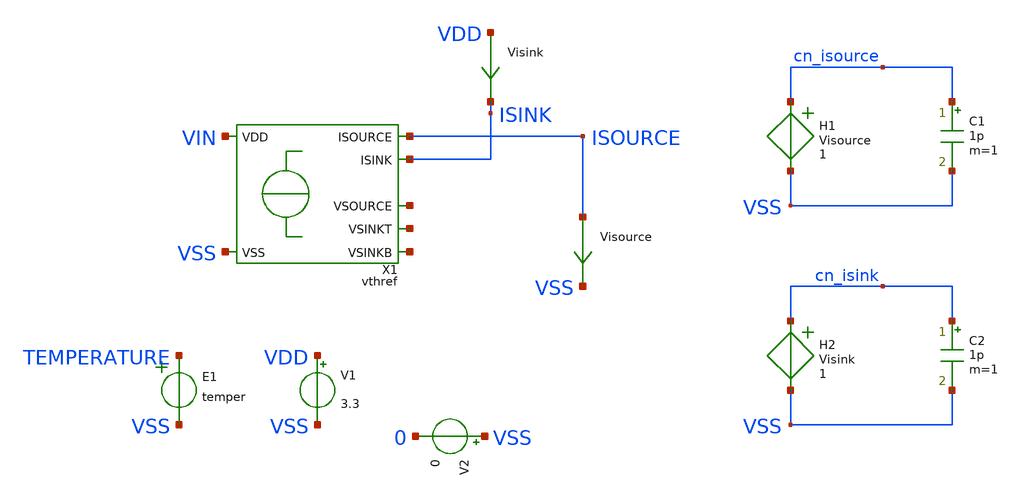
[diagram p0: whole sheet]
** sch_path: ip/vthref/xschem/vthref_tb.sch
**.subckt vthref_tb
X1 VIN VSS ISOURCE ISINK net1 net3 net2 vthref
V1 VDD VSS 3.3
Visink VDD ISINK 0
.save i(visink)
Visource ISOURCE VSS 0
.save i(visource)
V2 VSS 0 0
C1 cn_isource VSS 1p m=1
C2 cn_isink VSS 1p m=1
H1 cn_isource VSS Visource 1
H2 cn_isink VSS Visink 1
E1 TEMPERATURE VSS VOL=' temper '
**** begin user architecture code


.csparam TB_ID=${::TB_ID}
.csparam MC_RUNS=${::MC_RUNS}
.csparam EXIT_NGSPICE=${::EXIT_NGSPICE}
.lib ${::IHP_MODELS}/sg13g2.lib ${::CORNER}



* this experimental option enables mos model bin
* selection based on W/NF instead of W
.option wnflag=0

Vac1 VIN VDD 0.0 AC 1

Vdummy Vsweep VSS 0.0

.nodeset v(x1.vp)=1.0
.nodeset v(x1.vth)=0.22
.nodeset v(x1.vm)=0.840
.nodeset v(x1.vs)=0.006

.control
* option savecurrents
save all


* dummy block for goto
if (1)
if TB_ID = 0
	goto DC
end
if TB_ID = 1
	goto DC
end
if TB_ID = 2
	goto SINK_NOISE
end
if TB_ID = 3
	goto SOURCE_NOISE
end
if TB_ID = 4
	goto TRAN_STARTUP
end
if TB_ID = 5
	goto DC_PEX
end

****************************************
label DC
save all @n.x1.xmvth.nsg13_lv_nmos[ise] @n.x1.xmsul.nsg13_hv_nmos[ide] @n.x1.xmfb.nsg13_hv_nmos[ise]
.include vthref.inc
label DC_PEX
*save all
****************************************
if MC_RUNS = 0
	let veclen=3
	let source_pp = vector(veclen)
	let sink_pp = vector(veclen)
	let source_min = vector(veclen)
	let source_max = vector(veclen)
	let sink_min = vector(veclen)
	let sink_max = vector(veclen)
	let myvdd = vector(veclen)
	let idx = 0
	foreach v_sweep 1.8 2.5 3.3
	*foreach v_sweep 2.5
  		alter v1=$v_sweep
		option reltol=0.0001
  		dc temp -40 125 1
  		plot visource#branch
  		plot visink#branch
  		*plot x1.vth
  		*plot x1.vp
  		*plot x1.vm
		*plot x1.vs
		plot v.x1.vmeas#branch v.x1.vmeas1#branch
		*plot v.x1.vmeas2#branch
		*plot -1*@n.x1.xmvth.nsg13_lv_nmos[ise] @n.x1.xmsul.nsg13_hv_nmos[ide]
+ -1*@n.x1.xmfb.nsg13_hv_nmos[ise]
		*plot @n.x1.xmvth.nsg13_lv_nmos[vds] @n.x1.xmfb.nsg13_hv_nmos[vds]
+ @n.x1.xmmir1l.nsg13_hv_pmos[vds] @n.x1.xmmir1r.nsg13_hv_pmos[vds]
		let source_min[idx] = minimum(visource#branch)
		let source_max[idx] = maximum(visource#branch)
		let source_pp[idx] = maximum(visource#branch)-minimum(visource#branch)
		let sink_min[idx] = minimum(visink#branch)
		let sink_max[idx] = maximum(visink#branch)
		let sink_pp[idx] = maximum(visink#branch)-minimum(visink#branch)
		let myvdd[idx] = $v_sweep
		let idx = idx + 1
		*echo ISOURCE span: $&source_pp[idx]
		*echo ISINK span: $&sink_pp[idx]
		write dc.raw all
		set appendwrite
	end
	set nobreak
	set width=300
	print myvdd, source_pp, sink_pp, source_min, source_max, sink_min, sink_max > dc.csv
else
	let source_pp = vector(MC_RUNS)
	let sink_pp = vector(MC_RUNS)
	let source_min = vector(MC_RUNS)
	let source_max = vector(MC_RUNS)
	let sink_min = vector(MC_RUNS)
	let sink_max = vector(MC_RUNS)
	let run=0
	dowhile run < MC_RUNS
		echo MC-RUN: $&run
		alter v1=aunif(2.55,0.75)
		option reltol=0.0001
		dc temp -40 140 1
		let source_min[run] = minimum(visource#branch)
		let source_max[run] = maximum(visource#branch)
		let source_pp[run] = maximum(visource#branch)-minimum(visource#branch)
		let sink_min[run] = minimum(visink#branch)
		let sink_max[run] = maximum(visink#branch)
		let sink_pp[run] = maximum(visink#branch)-minimum(visink#branch)
  		*plot visource#branch
		*plot visink#branch
		*write dc_CID_{$&CORNER_ID}_MC_{$&run}.raw all
 		reset
		let run = run + 1
	end
	set nobreak
	set width=300
	print source_pp, sink_pp, source_min, source_max, sink_min, sink_max > dc.csv
end
goto done

****************************************
label SOURCE_NOISE
****************************************
noise v(cn_isource) Vac1 dec 10 1 100e3 1
setplot noise2
print onoise_total
setplot noise1
plot onoise_spectrum
write noise1_isource.raw all
goto done

****************************************
label SINK_NOISE
****************************************
noise v(cn_isink) Vac1 dec 10 1 100e3 1
setplot noise2
print onoise_total
setplot noise1
plot onoise_spectrum loglog
write noise1_isink.raw all
goto done

****************************************
label TRAN_STARTUP
****************************************
if MC_RUNS = 0
	let veclen=3
	let startup_t = vector(veclen)
	let run=0
	foreach v_sweep 1.8 2.5 3.3
	*foreach v_sweep 3.3
		save all
		alter vdummy=$v_sweep
		alter @v1[pwl] = [ 0 0 1u 0 10u $v_sweep]
  		tran 10n 100u
  		plot visource#branch
  		plot visink#branch
		plot VDD
		meas tran m_cur_up when i(visource)=1e-6 rise=1
		let startup_t[run] = m_cur_up
		write tran.raw all
		let run = run + 1
		set appendwrite
		reset
	end
	print startup_t > tran.csv
else
	let startup_t = vector(MC_RUNS)
	let run=0
	dowhile run < MC_RUNS
		echo MC-RUN: $&run
		alter @v1[pwl] = [ 0 0 1u 0 10u 3.3]
		tran 10n 100u
		meas tran m_cur_up when i(visource)=1e-6 rise=1
		let startup_t[run] = m_cur_up
 		reset
		let run = run + 1
	end
	print startup_t > tran.csv
end
goto done

****************************************
label done
****************************************
if EXIT_NGSPICE > 0.0
	exit
end
end
.endc


**** end user architecture code
**.ends

* expanding   symbol:  vthref.sym # of pins=7
** sym_path: ip/vthref/xschem/vthref.sym
** sch_path: ip/vthref/xschem/vthref.sch
.subckt vthref VDD VSS ISOURCE ISINK VSOURCE VSINKT VSINKB
*.iopin VSS
*.iopin VDD
*.ipin ISINK
*.opin ISOURCE
*.iopin VSOURCE
*.iopin VSINKT
*.iopin VSINKB
XMMIR1L vp vm VDD VDD sg13_hv_pmos w=10u l=15u ng=1 m=6 mm_ok=1
XMMIR1R vm vm VDD VDD sg13_hv_pmos w=10u l=15u ng=1 m=6 mm_ok=1
XMSIT net2 vm VDD VDD sg13_hv_pmos w=10u l=15u ng=1 m=6 mm_ok=1
XMSOTL VSOURCE VSOURCE VDD VDD sg13_hv_pmos w=10u l=15u ng=1 m=6 mm_ok=1
XMSOTR ISOURCE VSOURCE VDD VDD sg13_hv_pmos w=10u l=15u ng=1 m=6 mm_ok=1
XMFB vm vp vth VSS sg13_hv_nmos w=5u l=16u ng=1 m=13 mm_ok=1
XMVTH vp vth net1 VSS sg13_lv_nmos w=5u l=16u ng=1 m=13 mm_ok=1
XMMB1 VSINKB VSINKB VSS VSS sg13_lv_nmos w=10u l=15u ng=1 m=6 mm_ok=1
XMMB2 vm2 VSINKB VSS VSS sg13_lv_nmos w=10u l=15u ng=1 m=6 mm_ok=1
XMMB3 vm3 VSINKB VSS VSS sg13_lv_nmos w=10u l=15u ng=1 m=6 mm_ok=1
XMMCB1 VSINKT VSINKT VSINKB VSS sg13_hv_nmos w=10u l=2u ng=1 m=4 mm_ok=1
XMMCB2 ISINK VSINKT vm2 VSS sg13_hv_nmos w=10u l=2u ng=1 m=4 mm_ok=1
XMMCB3 VSOURCE VSINKT vm3 VSS sg13_hv_nmos w=10u l=2u ng=1 m=4 mm_ok=1
XMSUL vs vp VSS VSS sg13_hv_nmos w=10u l=0.5u ng=1 m=1 mm_ok=1
Vmeas net1 VSS 0
.save i(vmeas)
Vmeas1 vth net3 0
.save i(vmeas1)
Vmeas2 net2 VSINKT 0
.save i(vmeas2)
XDSU vs vp dpantenna l=5u w=5u
XRSU VDD vs VSS rhigh w=0.5e-6 l=110e-6 m=1 b=0 mm_ok=1
XR1 net3 VSS VSS rhigh w=0.5e-6 l=12e-6 m=1 b=0 mm_ok=1
.ends

.end
